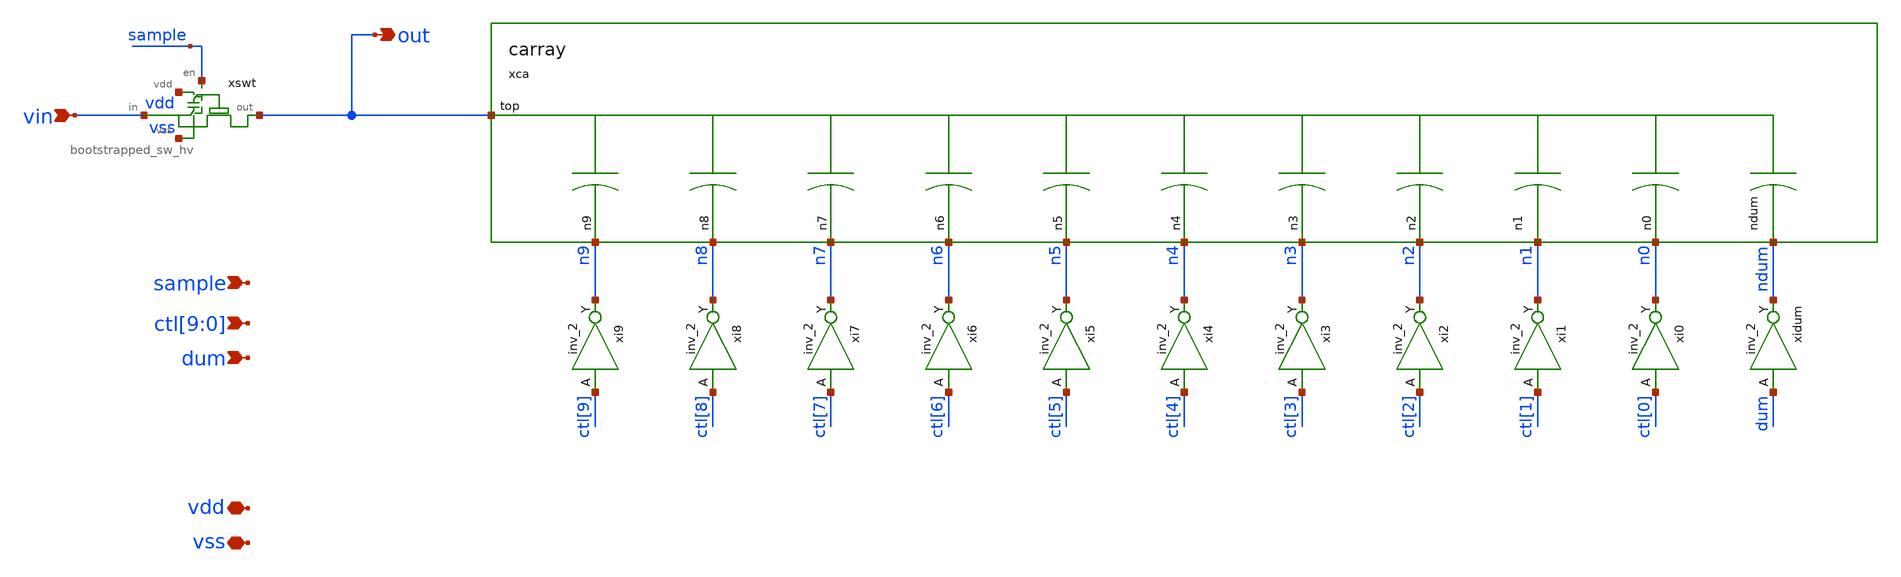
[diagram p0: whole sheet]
** sch_path: check/xschem/sar_10b/dac/dac.sch
**.subckt dac vin sample out ctl[9],ctl[8],ctl[7],ctl[6],ctl[5],ctl[4],ctl[3],ctl[2],ctl[1],ctl[0]
*+ dum vdd vss
*.ipin vin
*.ipin sample
*.opin out
*.ipin ctl[9],ctl[8],ctl[7],ctl[6],ctl[5],ctl[4],ctl[3],ctl[2],ctl[1],ctl[0]
*.ipin dum
*.iopin vdd
*.iopin vss
xca out n6 n0 n5 n4 n2 ndum n3 n1 n7 n8 n9 carray
xswt out sample vdd vin vss bootstrapped_sw_hv
xidum dum vss vss vdd vdd ndum sky130_fd_sc_hd__inv_2
xi0 ctl[0] vss vss vdd vdd n0 sky130_fd_sc_hd__inv_2
xi1 ctl[1] vss vss vdd vdd n1 sky130_fd_sc_hd__inv_2
xi2 ctl[2] vss vss vdd vdd n2 sky130_fd_sc_hd__inv_2
xi3 ctl[3] vss vss vdd vdd n3 sky130_fd_sc_hd__inv_2
xi4 ctl[4] vss vss vdd vdd n4 sky130_fd_sc_hd__inv_2
xi5 ctl[5] vss vss vdd vdd n5 sky130_fd_sc_hd__inv_2
xi6 ctl[6] vss vss vdd vdd n6 sky130_fd_sc_hd__inv_2
xi7 ctl[7] vss vss vdd vdd n7 sky130_fd_sc_hd__inv_2
xi8 ctl[8] vss vss vdd vdd n8 sky130_fd_sc_hd__inv_2
xi9 ctl[9] vss vss vdd vdd n9 sky130_fd_sc_hd__inv_2
**.ends
.end
